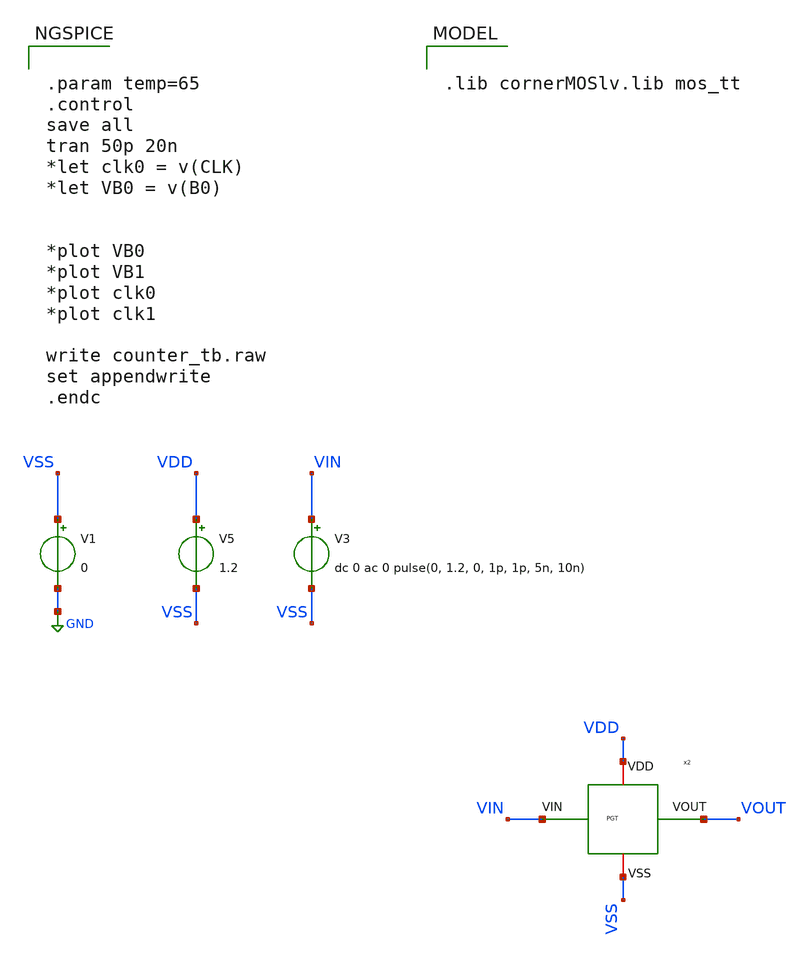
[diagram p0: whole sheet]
** sch_path: ADC8711-main/testbenches/tran/xschem/tb_PGT.sch
**.subckt tb_PGT
V1 VSS GND 0
V3 VIN VSS dc 0 ac 0 pulse(0, 1.2, 0, 1p, 1p, 5n, 10n)
V5 VDD VSS 1.2
x2 VDD VIN VOUT VSS PGT
**** begin user architecture code


.param temp=65
.control
save all
tran 50p 20n
*let clk0 = v(CLK)
*let VB0 = v(B0)


*plot VB0
*plot VB1
*plot clk0
*plot clk1

write counter_tb.raw
set appendwrite
.endc



.lib cornerMOSlv.lib mos_tt

**** end user architecture code
**.ends
.GLOBAL GND
.end
